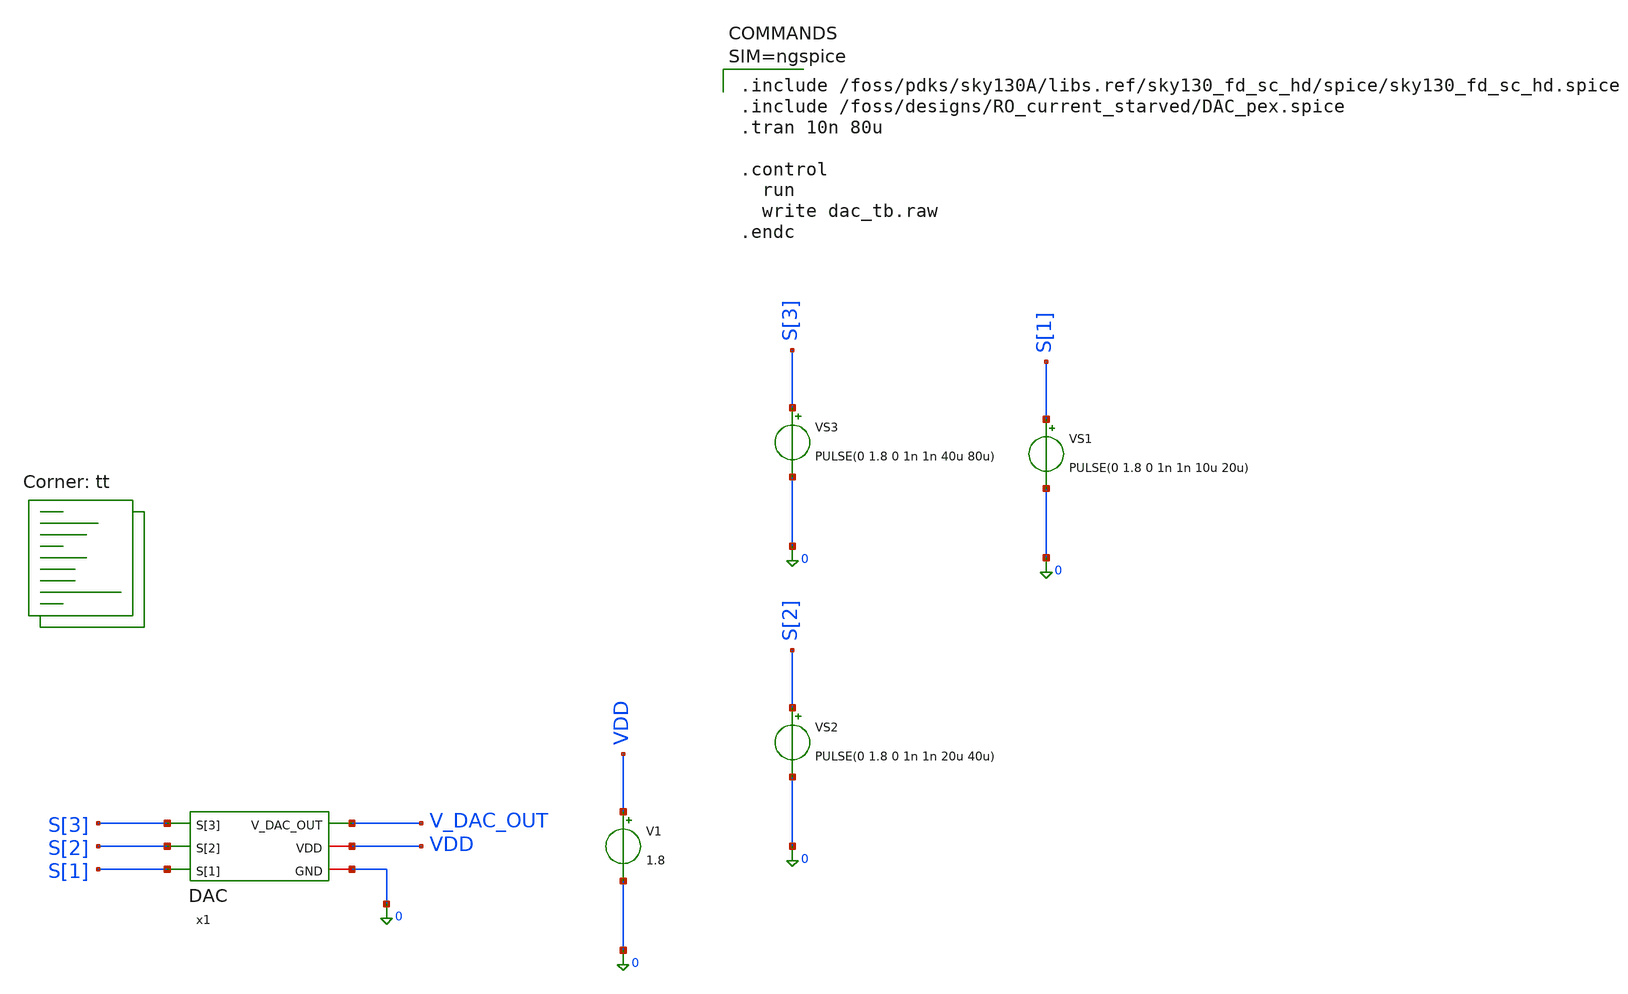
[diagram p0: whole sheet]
** sch_path: src/analog_source_files/DAC_tb.sch
**.subckt DAC_tb
x1 S[3] S[1] S[2] V_DAC_OUT VDD 0 DAC
V1 VDD 0 1.8
VS1 S[1] 0 PULSE(0 1.8 0 1n 1n 10u 20u)
VS2 S[2] 0 PULSE(0 1.8 0 1n 1n 20u 40u)
VS3 S[3] 0 PULSE(0 1.8 0 1n 1n 40u 80u)
**** begin user architecture code
.lib $::SKYWATER_MODELS/sky130.lib.spice tt


.include /foss/pdks/sky130A/libs.ref/sky130_fd_sc_hd/spice/sky130_fd_sc_hd.spice
.include /foss/designs/RO_current_starved/DAC_pex.spice
.tran 10n 80u

.control
  run
  write dac_tb.raw
.endc



**** end user architecture code
**.ends

* expanding   symbol:  DAC.sym # of pins=6
** sym_path: src/analog_source_files/DAC.sym
** sch_path: src/analog_source_files/DAC.sch
.subckt DAC S[3] S[1] S[2] V_DAC_OUT VDD GND
*.ipin S[1]
*.ipin S[2]
*.ipin S[3]
*.iopin VDD
*.iopin GND
*.opin V_DAC_OUT
XR1 net2 net1 GND sky130_fd_pr__res_xhigh_po_0p35 L=1 mult=1 m=1
XR2 net1 VDD GND sky130_fd_pr__res_xhigh_po_0p35 L=1 mult=1 m=1
XR3 net4 net3 GND sky130_fd_pr__res_xhigh_po_0p35 L=1 mult=1 m=1
XR4 net3 net2 GND sky130_fd_pr__res_xhigh_po_0p35 L=1 mult=1 m=1
XR5 net6 net5 GND sky130_fd_pr__res_xhigh_po_0p35 L=1 mult=1 m=1
XR6 net5 net4 GND sky130_fd_pr__res_xhigh_po_0p35 L=1 mult=1 m=1
XR7 GND net7 GND sky130_fd_pr__res_xhigh_po_0p35 L=1 mult=1 m=1
XR8 net7 net6 GND sky130_fd_pr__res_xhigh_po_0p35 L=1 mult=1 m=1
x1 S[1] net1 net8 net2 VDD GND SELECTOR
x2 S[1] net3 net9 net4 VDD GND SELECTOR
x3 S[1] net5 net10 net6 VDD GND SELECTOR
x4 S[1] net7 net11 GND VDD GND SELECTOR
x5 S[2] net8 net12 net9 VDD GND SELECTOR
x6 S[2] net10 net13 net11 VDD GND SELECTOR
x7 S[3] net12 V_DAC_OUT net13 VDD GND SELECTOR
.ends


* expanding   symbol:  SELECTOR.sym # of pins=6
** sym_path: src/analog_source_files/SELECTOR.sym
** sch_path: src/analog_source_files/SELECTOR.sch
.subckt SELECTOR CONTROL N1 OUT P1 VDD GND
*.ipin N1
*.ipin P1
*.ipin CONTROL
*.opin OUT
*.iopin VDD
*.iopin GND
x1 CONTROL OUT N1 VDD GND transmition_gate
x2 net1 OUT P1 VDD GND transmition_gate
x3 CONTROL GND GND VDD VDD net1 sky130_fd_sc_hd__inv_1
.ends


* expanding   symbol:  transmition_gate.sym # of pins=5
** sym_path: src/analog_source_files/transmition_gate.sym
** sch_path: src/analog_source_files/transmition_gate.sch
.subckt transmition_gate CONTROL OUT IN VDD GND
*.ipin IN
*.ipin CONTROL
*.opin OUT
*.iopin VDD
*.iopin GND
XM2 IN net1 OUT VDD sky130_fd_pr__pfet_01v8 L=0.15 W=1 nf=1 ad='int((1 + 1)/2) * 1 / 1 * 0.29' as='int((1 + 2)/2) * 1 / 1 * 0.29'
+ pd='2*int((1 + 1)/2) * (1 / 1 + 0.29)' ps='2*int((1 + 2)/2) * (1 / 1 + 0.29)' nrd='0.29 / 1 ' nrs='0.29 / 1 '
+ sa=0 sb=0 sd=0 mult=1 m=1
x1 CONTROL GND GND VDD VDD net1 sky130_fd_sc_hd__inv_1
XM3 IN CONTROL OUT GND sky130_fd_pr__nfet_01v8 L=0.15 W=1 nf=1 ad='int((1 + 1)/2) * 1 / 1 * 0.29' as='int((1 + 2)/2) * 1 / 1 * 0.29'
+ pd='2*int((1 + 1)/2) * (1 / 1 + 0.29)' ps='2*int((1 + 2)/2) * (1 / 1 + 0.29)' nrd='0.29 / 1 ' nrs='0.29 / 1 '
+ sa=0 sb=0 sd=0 mult=1 m=1
.ends

.GLOBAL GND
.end
